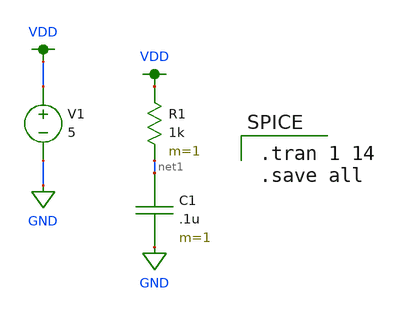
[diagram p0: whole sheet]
** sch_path: PS3.sch
**.subckt PS3
R1 VDD net1 1k m=1
V1 VDD GND 5
C1 net1 GND .1u m=1
**** begin user architecture code

.option wnflag=1
.lib ~/skywater/skywater-pdk/libraries/sky130_fd_pr_ngspice/latest/models/sky130.lib.spice tt


.tran 1 14
.save all

**** end user architecture code
**.ends
.GLOBAL GND
.GLOBAL VDD
.end
